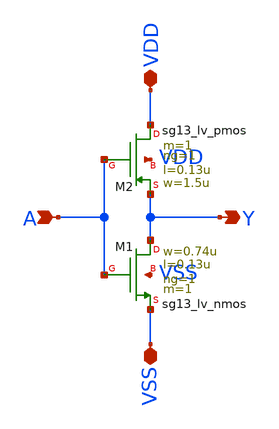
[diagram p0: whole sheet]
** sch_path: examples/ihp-inv/libs/cells/inv/schematic/inv.sch
**.subckt inv A Y VDD VSS
*.ipin A
*.opin Y
*.iopin VDD
*.iopin VSS
XM2 VDD A Y VDD sg13_lv_pmos w=1.5u l=0.13u ng=1 m=1 mm_ok=1
XM1 Y A VSS VSS sg13_lv_nmos w=0.74u l=0.13u ng=1 m=1 mm_ok=1
**.ends
.end
